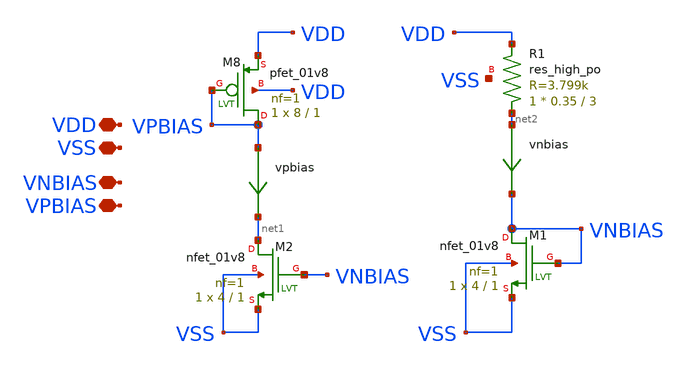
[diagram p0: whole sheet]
** sch_path: tt_um_emilian_rf_playground/xschem/vbias1.sch
**.subckt vbias1 VDD VSS VPBIAS VNBIAS
*.iopin VDD
*.iopin VSS
*.iopin VPBIAS
*.iopin VNBIAS
XR1 net2 VDD VSS sky130_fd_pr__res_high_po W=0.35 L=3 mult=1 m=1
XM8 VPBIAS VPBIAS VDD VDD sky130_fd_pr__pfet_01v8 L=1 W=8 nf=1 ad='int((nf+1)/2) * W/nf * 0.29' as='int((nf+2)/2) * W/nf * 0.29'
+ pd='2*int((nf+1)/2) * (W/nf + 0.29)' ps='2*int((nf+2)/2) * (W/nf + 0.29)' nrd='0.29 / W' nrs='0.29 / W'
+ sa=0 sb=0 sd=0 mult=1 m=1
vnbias net2 VNBIAS 0
.save i(vnbias)
vpbias VPBIAS net1 0
.save i(vpbias)
XM1 VNBIAS VNBIAS VSS VSS sky130_fd_pr__nfet_01v8 L=1 W=4 nf=1 ad='int((nf+1)/2) * W/nf * 0.29' as='int((nf+2)/2) * W/nf * 0.29'
+ pd='2*int((nf+1)/2) * (W/nf + 0.29)' ps='2*int((nf+2)/2) * (W/nf + 0.29)' nrd='0.29 / W' nrs='0.29 / W'
+ sa=0 sb=0 sd=0 mult=1 m=1
XM2 net1 VNBIAS VSS VSS sky130_fd_pr__nfet_01v8 L=1 W=4 nf=1 ad='int((nf+1)/2) * W/nf * 0.29' as='int((nf+2)/2) * W/nf * 0.29'
+ pd='2*int((nf+1)/2) * (W/nf + 0.29)' ps='2*int((nf+2)/2) * (W/nf + 0.29)' nrd='0.29 / W' nrs='0.29 / W'
+ sa=0 sb=0 sd=0 mult=1 m=1
**.ends
.end
